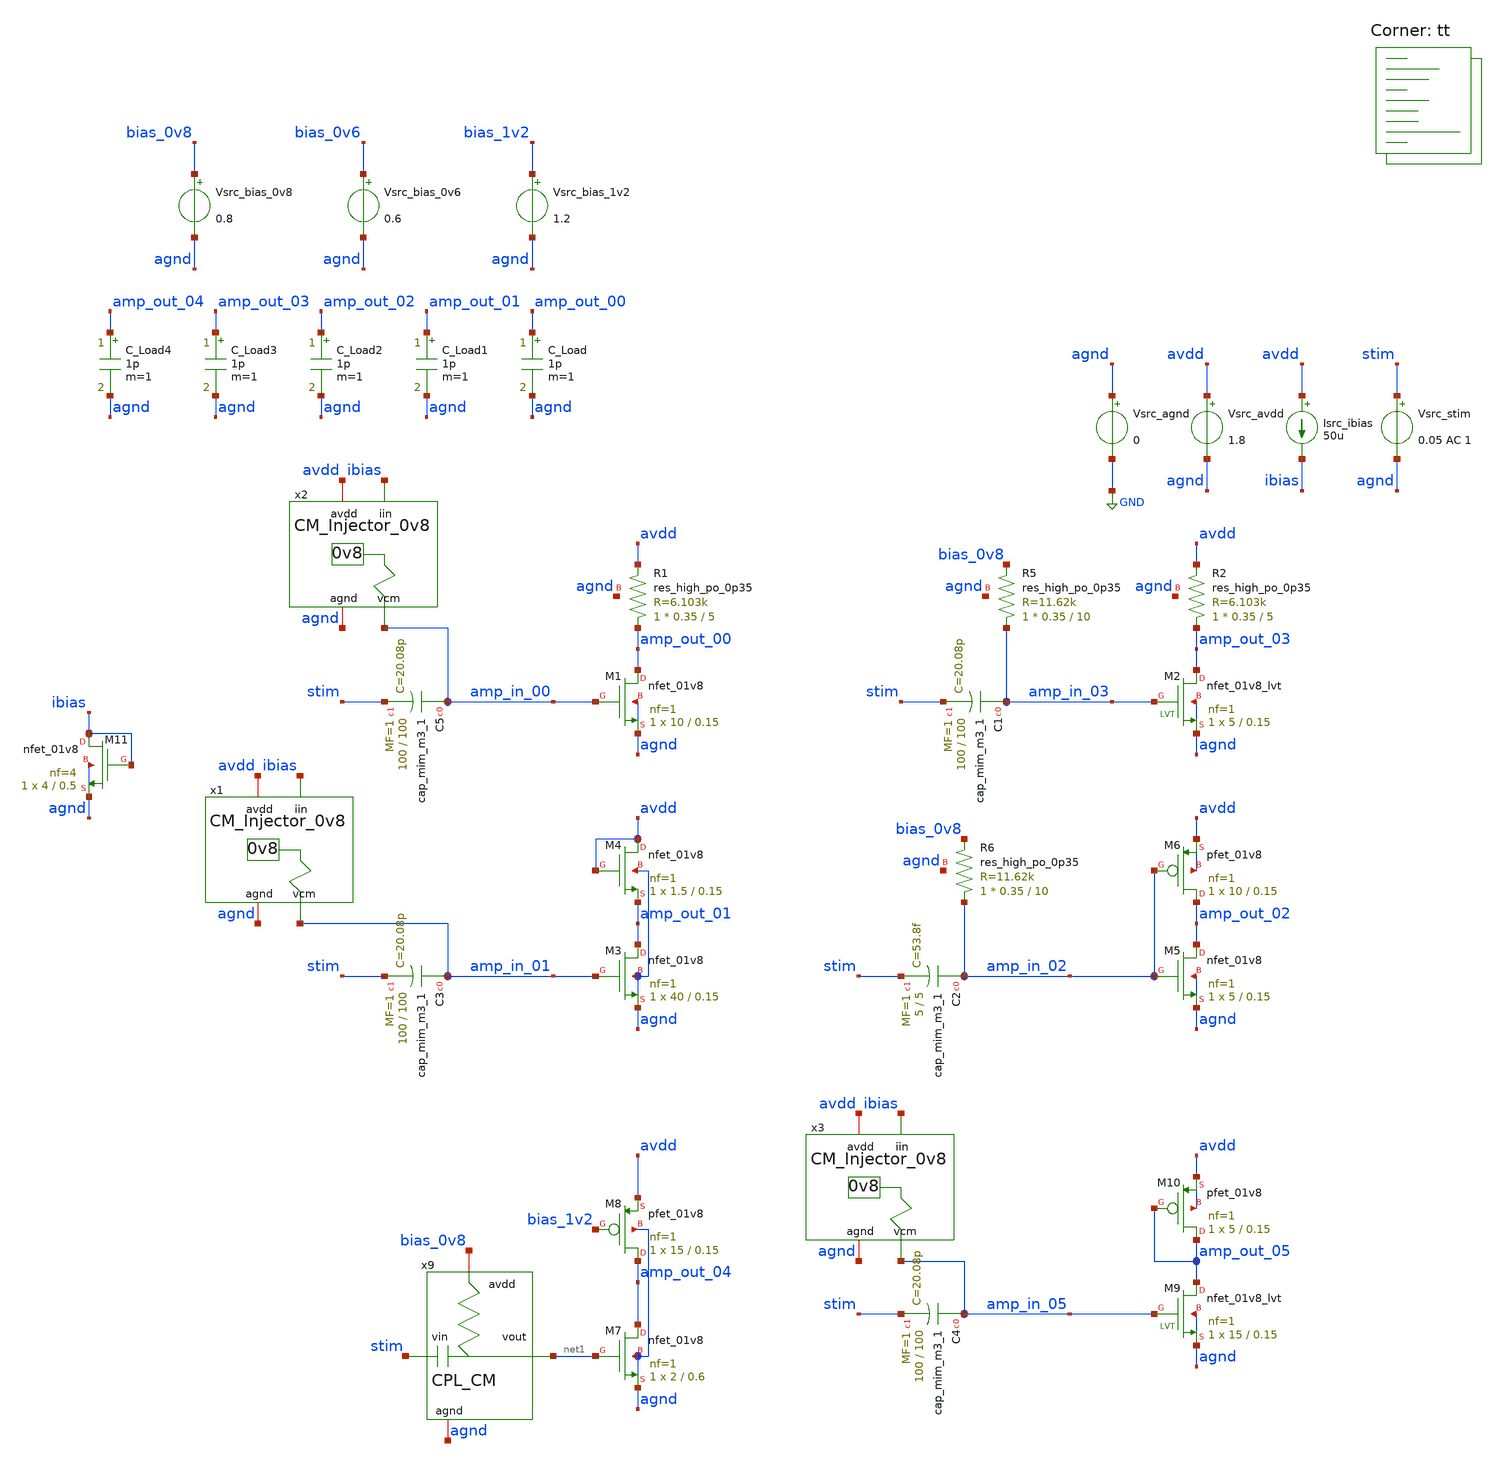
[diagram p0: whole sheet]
** sch_path: AMP/TB_Topologies.sch
**.subckt TB_Topologies
Vsrc_agnd agnd GND 0
Vsrc_avdd avdd agnd 1.8
Vsrc_stim stim agnd 0.05 AC 1
Isrc_ibias avdd ibias 50u
Vsrc_bias_1v2 bias_1v2 agnd 1.2
XM1 amp_out_00 amp_in_00 agnd agnd sky130_fd_pr__nfet_01v8 L=0.15 W=10 nf=1 ad='int((nf+1)/2) * W/nf * 0.29'
+ as='int((nf+2)/2) * W/nf * 0.29' pd='2*int((nf+1)/2) * (W/nf + 0.29)' ps='2*int((nf+2)/2) * (W/nf + 0.29)'
+ nrd='0.29 / W' nrs='0.29 / W' sa=0 sb=0 sd=0 mult=1 m=1
XR1 amp_out_00 avdd agnd sky130_fd_pr__res_high_po_0p35 L=5 mult=1 m=1
C_Load amp_out_00 agnd 1p m=1
XM3 amp_out_01 amp_in_01 agnd agnd sky130_fd_pr__nfet_01v8 L=0.15 W=40 nf=1 ad='int((nf+1)/2) * W/nf * 0.29'
+ as='int((nf+2)/2) * W/nf * 0.29' pd='2*int((nf+1)/2) * (W/nf + 0.29)' ps='2*int((nf+2)/2) * (W/nf + 0.29)'
+ nrd='0.29 / W' nrs='0.29 / W' sa=0 sb=0 sd=0 mult=1 m=1
XM4 avdd avdd amp_out_01 agnd sky130_fd_pr__nfet_01v8 L=0.15 W=1.5 nf=1 ad='int((nf+1)/2) * W/nf * 0.29'
+ as='int((nf+2)/2) * W/nf * 0.29' pd='2*int((nf+1)/2) * (W/nf + 0.29)' ps='2*int((nf+2)/2) * (W/nf + 0.29)'
+ nrd='0.29 / W' nrs='0.29 / W' sa=0 sb=0 sd=0 mult=1 m=1
C_Load1 amp_out_01 agnd 1p m=1
XM6 amp_out_02 amp_in_02 avdd avdd sky130_fd_pr__pfet_01v8 L=0.15 W=10 nf=1 ad='int((nf+1)/2) * W/nf * 0.29'
+ as='int((nf+2)/2) * W/nf * 0.29' pd='2*int((nf+1)/2) * (W/nf + 0.29)' ps='2*int((nf+2)/2) * (W/nf + 0.29)'
+ nrd='0.29 / W' nrs='0.29 / W' sa=0 sb=0 sd=0 mult=1 m=1
XR2 amp_out_03 avdd agnd sky130_fd_pr__res_high_po_0p35 L=5 mult=1 m=1
XM2 amp_out_03 amp_in_03 agnd agnd sky130_fd_pr__nfet_01v8_lvt L=0.15 W=5 nf=1 ad='int((nf+1)/2) * W/nf * 0.29'
+ as='int((nf+2)/2) * W/nf * 0.29' pd='2*int((nf+1)/2) * (W/nf + 0.29)' ps='2*int((nf+2)/2) * (W/nf + 0.29)'
+ nrd='0.29 / W' nrs='0.29 / W' sa=0 sb=0 sd=0 mult=1 m=1
C_Load2 amp_out_02 agnd 1p m=1
C_Load3 amp_out_03 agnd 1p m=1
C_Load4 amp_out_04 agnd 1p m=1
XM7 amp_out_04 net1 agnd agnd sky130_fd_pr__nfet_01v8 L=0.6 W=2 nf=1 ad='int((nf+1)/2) * W/nf * 0.29'
+ as='int((nf+2)/2) * W/nf * 0.29' pd='2*int((nf+1)/2) * (W/nf + 0.29)' ps='2*int((nf+2)/2) * (W/nf + 0.29)'
+ nrd='0.29 / W' nrs='0.29 / W' sa=0 sb=0 sd=0 mult=1 m=1
Vsrc_bias_0v6 bias_0v6 agnd 0.6
x9 bias_0v8 agnd net1 stim CPL_CM
Vsrc_bias_0v8 bias_0v8 agnd 0.8
XC5 amp_in_00 stim sky130_fd_pr__cap_mim_m3_1 W=100 L=100 MF=1 m=1
XR5 amp_in_03 bias_0v8 agnd sky130_fd_pr__res_high_po_0p35 L=10 mult=1 m=1
XC1 amp_in_03 stim sky130_fd_pr__cap_mim_m3_1 W=100 L=100 MF=1 m=1
XR6 amp_in_02 bias_0v8 agnd sky130_fd_pr__res_high_po_0p35 L=10 mult=1 m=1
XC2 amp_in_02 stim sky130_fd_pr__cap_mim_m3_1 W=5 L=5 MF=1 m=1
XC3 amp_in_01 stim sky130_fd_pr__cap_mim_m3_1 W=100 L=100 MF=1 m=1
XM10 amp_out_05 amp_out_05 avdd avdd sky130_fd_pr__pfet_01v8 L=0.15 W=5 nf=1 ad='int((nf+1)/2) * W/nf * 0.29'
+ as='int((nf+2)/2) * W/nf * 0.29' pd='2*int((nf+1)/2) * (W/nf + 0.29)' ps='2*int((nf+2)/2) * (W/nf + 0.29)'
+ nrd='0.29 / W' nrs='0.29 / W' sa=0 sb=0 sd=0 mult=1 m=1
XM9 amp_out_05 amp_in_05 agnd agnd sky130_fd_pr__nfet_01v8_lvt L=0.15 W=15 nf=1 ad='int((nf+1)/2) * W/nf * 0.29'
+ as='int((nf+2)/2) * W/nf * 0.29' pd='2*int((nf+1)/2) * (W/nf + 0.29)' ps='2*int((nf+2)/2) * (W/nf + 0.29)'
+ nrd='0.29 / W' nrs='0.29 / W' sa=0 sb=0 sd=0 mult=1 m=1
XM5 amp_out_02 amp_in_02 agnd agnd sky130_fd_pr__nfet_01v8 L=0.15 W=5 nf=1 ad='int((nf+1)/2) * W/nf * 0.29'
+ as='int((nf+2)/2) * W/nf * 0.29' pd='2*int((nf+1)/2) * (W/nf + 0.29)' ps='2*int((nf+2)/2) * (W/nf + 0.29)'
+ nrd='0.29 / W' nrs='0.29 / W' sa=0 sb=0 sd=0 mult=1 m=1
XM8 amp_out_04 bias_1v2 avdd agnd sky130_fd_pr__pfet_01v8 L=0.15 W=15 nf=1 ad='int((nf+1)/2) * W/nf * 0.29'
+ as='int((nf+2)/2) * W/nf * 0.29' pd='2*int((nf+1)/2) * (W/nf + 0.29)' ps='2*int((nf+2)/2) * (W/nf + 0.29)'
+ nrd='0.29 / W' nrs='0.29 / W' sa=0 sb=0 sd=0 mult=1 m=1
x1 avdd amp_in_01 ibias agnd CM_Injector_0v8
XM11 ibias ibias agnd agnd sky130_fd_pr__nfet_01v8 L=0.5 W=4 nf=4 ad='int((nf+1)/2) * W/nf * 0.29' as='int((nf+2)/2) * W/nf * 0.29'
+ pd='2*int((nf+1)/2) * (W/nf + 0.29)' ps='2*int((nf+2)/2) * (W/nf + 0.29)' nrd='0.29 / W' nrs='0.29 / W'
+ sa=0 sb=0 sd=0 mult=1 m=1
x2 avdd amp_in_00 ibias agnd CM_Injector_0v8
XC4 amp_in_05 stim sky130_fd_pr__cap_mim_m3_1 W=100 L=100 MF=1 m=1
x3 avdd amp_in_05 ibias agnd CM_Injector_0v8
**** begin user architecture code

* this option enables mos model bin
* selection based on W/NF instead of W

.option savecurrents

.control
save all
op

* Print newline
echo

* Store MOS lists
set nmos_list = ( xm1 xm3 xm4 xm5 xm7 )
set pmos_list = ( xm6 xm8 xm10 )
set nmos_lvt_list = ( xm2 xm9 )
set pmos_lvt_list = (  )

* Print stats for each MOSFET
foreach nmos $nmos_list
 * Save stats
 save @m.{$nmos}.msky130_fd_pr__nfet_01v8[gm]
 let vth   = @m.{$nmos}.msky130_fd_pr__nfet_01v8[vth]
 let vgs   = @m.{$nmos}.msky130_fd_pr__nfet_01v8[vgs]
 let vds   = @m.{$nmos}.msky130_fd_pr__nfet_01v8[vds]
 let vdsat = @m.{$nmos}.msky130_fd_pr__nfet_01v8[vdsat]
 let gm    = @m.{$nmos}.msky130_fd_pr__nfet_01v8[gm]
 let gds   = @m.{$nmos}.msky130_fd_pr__nfet_01v8[gds]


 * Print stats
 echo Stats for $nmos:
 print vth
 print vgs
 print vds
 print vdsat
 print gm
 print gds

 * Print newline
 echo
end

foreach pmos $pmos_list
 * Save stats
 save @m.{$pmos}.msky130_fd_pr__nfet_01v8[gm]
 let vth   = @m.{$pmos}.msky130_fd_pr__pfet_01v8[vth]
 let vgs   = @m.{$pmos}.msky130_fd_pr__pfet_01v8[vgs]
 let vds   = @m.{$pmos}.msky130_fd_pr__pfet_01v8[vds]
 let vdsat = @m.{$pmos}.msky130_fd_pr__pfet_01v8[vdsat]
 let gm    = @m.{$pmos}.msky130_fd_pr__pfet_01v8[gm]
 let gds   = @m.{$pmos}.msky130_fd_pr__pfet_01v8[gds]

 * Print stats
 echo Stats for $pmos:
 print vth
 print vgs
 print vds
 print vdsat
 print gm
 print gds

 * Print newline
 echo
end

foreach nmos_lvt $nmos_lvt_list
 * Save stats
 save @m.{$nmos_lvt}.msky130_fd_pr__nfet_01v8_lvt[gm]
 let vth   = @m.{$nmos_lvt}.msky130_fd_pr__nfet_01v8_lvt[vth]
 let vgs   = @m.{$nmos_lvt}.msky130_fd_pr__nfet_01v8_lvt[vgs]
 let vds   = @m.{$nmos_lvt}.msky130_fd_pr__nfet_01v8_lvt[vds]
 let vdsat = @m.{$nmos_lvt}.msky130_fd_pr__nfet_01v8_lvt[vdsat]
 let gm    = @m.{$nmos_lvt}.msky130_fd_pr__nfet_01v8_lvt[gm]
 let gds   = @m.{$nmos_lvt}.msky130_fd_pr__nfet_01v8_lvt[gds]


 * Print stats
 echo Stats for $nmos_lvt:
 print vth
 print vgs
 print vds
 print vdsat
 print gm
 print gds

 * Print newline
 echo
end

foreach pmos_lvt $pmos_lvt_list
 * Save stats
 save @m.{$pmos_lvt}.msky130_fd_pr__nfet_01v8_lvt[gm]
 let vth   = @m.{$pmos_lvt}.msky130_fd_pr__pfet_01v8_lvt[vth]
 let vgs   = @m.{$pmos_lvt}.msky130_fd_pr__pfet_01v8_lvt[vgs]
 let vds   = @m.{$pmos_lvt}.msky130_fd_pr__pfet_01v8_lvt[vds]
 let vdsat = @m.{$pmos_lvt}.msky130_fd_pr__pfet_01v8_lvt[vdsat]
 let gm    = @m.{$pmos_lvt}.msky130_fd_pr__pfet_01v8_lvt[gm]
 let gds   = @m.{$pmos_lvt}.msky130_fd_pr__pfet_01v8_lvt[gds]


 * Print stats
 echo Stats for $pmos_lvt:
 print vth
 print vgs
 print vds
 print vdsat
 print gm
 print gds

 * Print newline
 echo
end

* Print region of operation
echo Regions of Operation:
echo

echo NMOS:
foreach nmos $nmos_list
 * Save stats
 let vds = @m.{$nmos}.msky130_fd_pr__nfet_01v8[vds]
 let vgs = @m.{$nmos}.msky130_fd_pr__nfet_01v8[vgs]
 let vth = @m.{$nmos}.msky130_fd_pr__nfet_01v8[vth]

 * Check and print regions
 if (vgs <= vth)
  echo $nmos: N Cutoff
  print vgs
  print vth
 end
 if (vgs > vth) & (vds <= (vgs - vth))
  echo $nmos: N Triode
  print vgs
  print vth
  print vds
 end
 if (vgs > vth) & (vds > (vgs - vth))
  echo $nmos: N Saturation
 end
end
echo

echo PMOS:
foreach pmos $pmos_list
 * Save stats
 let vds = @m.{$pmos}.msky130_fd_pr__pfet_01v8[vds]
 let vgs = @m.{$pmos}.msky130_fd_pr__pfet_01v8[vgs]
 let vth = @m.{$pmos}.msky130_fd_pr__pfet_01v8[vth]

 * Check and print regions
 if (abs(vgs) <= abs(vth))
  echo $pmos: P Cutoff
  print vgs
  print vth
 end
 if (abs(vgs) > abs(vth)) & (abs(vds) <= (abs(vgs) - abs(vth)))
  echo $pmos: P Triode
  print vgs
  print vth
  print vds
 end
 if (abs(vgs) > abs(vth)) & (abs(vds) > (abs(vgs) - abs(vth)))
  echo $pmos: P Saturation
 end
end
echo

echo NMOS_lvt:
foreach nmos_lvt $nmos_lvt_list
 * Save stats
 let vds = @m.{$nmos_lvt}.msky130_fd_pr__nfet_01v8_lvt[vds]
 let vgs = @m.{$nmos_lvt}.msky130_fd_pr__nfet_01v8_lvt[vgs]
 let vth = @m.{$nmos_lvt}.msky130_fd_pr__nfet_01v8_lvt[vth]

 * Check and print regions
 if (vgs <= vth)
  echo $nmos_lvt: N Cutoff
  print vgs
  print vth
 end
 if (vgs > vth) & (vds <= (vgs - vth))
  echo $nmos_lvt: N Triode
  print vgs
  print vth
  print vds
 end
 if (vgs > vth) & (vds > (vgs - vth))
  echo $nmos_lvt: N Saturation
 end
end
echo

echo PMOS_lvt:
foreach pmos_lvt $pmos_lvt_list
 * Save stats
 let vds = @m.{$pmos_lvt}.msky130_fd_pr__pfet_01v8_lvt[vds]
 let vgs = @m.{$pmos_lvt}.msky130_fd_pr__pfet_01v8_lvt[vgs]
 let vth = @m.{$pmos_lvt}.msky130_fd_pr__pfet_01v8_lvt[vth]

 * Check and print regions
 if (abs(vgs) <= abs(vth))
  echo $pmos_lvt: P Cutoff
  print vgs
  print vth
 end
 if (abs(vgs) > abs(vth)) & (abs(vds) <= (abs(vgs) - abs(vth)))
  echo $pmos_lvt: P Triode
  print vgs
  print vth
  print vds
 end
 if (abs(vgs) > abs(vth)) & (abs(vds) > (abs(vgs) - abs(vth)))
  echo $pmos_lvt: P Saturation
 end
end
echo

* Sweep frequency
write TB_Topologies.raw
set appendwrite
ac dec 200 1e0 1e11
remzerovec

* Calculate gain
let ratio_00 = v(amp_out_00)/v(stim)
let ratio_01 = v(amp_out_01)/v(stim)
let ratio_02 = v(amp_out_02)/v(stim)
let ratio_03 = v(amp_out_03)/v(stim)
let ratio_04 = v(amp_out_04)/v(stim)
let ratio_05 = v(amp_out_05)/v(stim)

let gain_00 = db(mag(ratio_00))
let gain_01 = db(mag(ratio_01))
let gain_02 = db(mag(ratio_02))
let gain_03 = db(mag(ratio_03))
let gain_04 = db(mag(ratio_04))
let gain_05 = db(mag(ratio_05))

write TB_Topologies.raw

.endc


.lib $::SKYWATER_MODELS/sky130.lib.spice tt
**** end user architecture code
**.ends
.GLOBAL GND
.end
